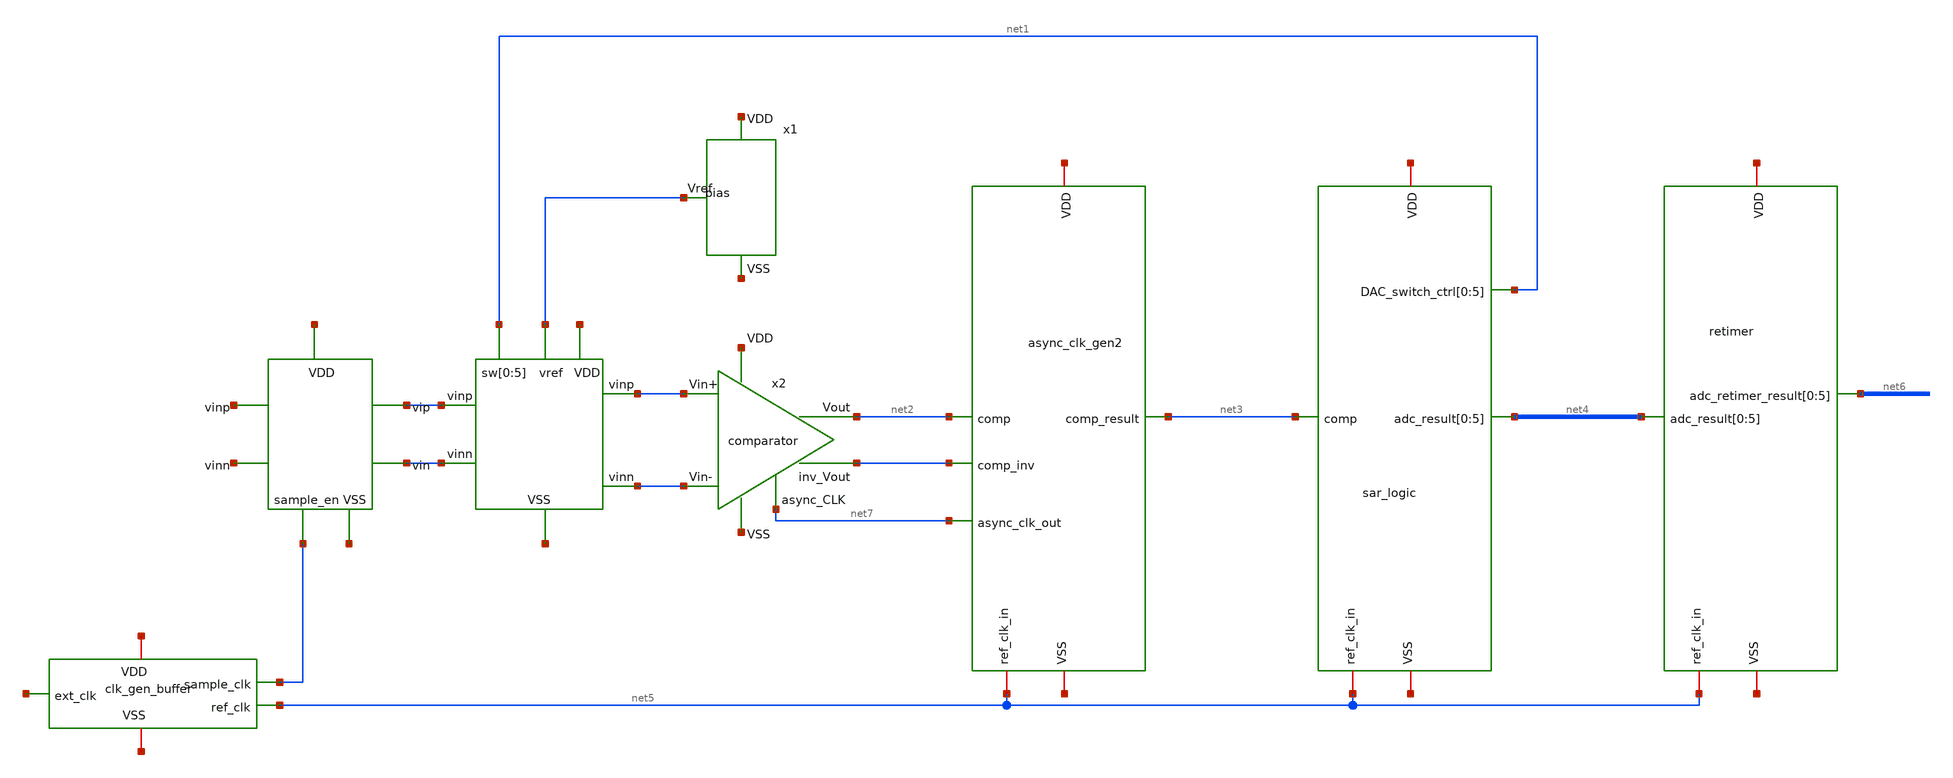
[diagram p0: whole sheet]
** sch_path: just_sym/6bit_SAR_ADC_top.sch
**.subckt 6bit_SAR_ADC_top
x1 net8 net9 net1 net10 net5 clk_gen_buffer
x1 net13 net14 net1 bias
x2 net1 net1 net15 net16 net2
x1 net19 net20 net3 net4[5] net4[4] net4[3] net4[2] net4[1] net4[0] net5 net1 net1 net1 net1 net1
+ net1 sar_logic
**.ends
.end
